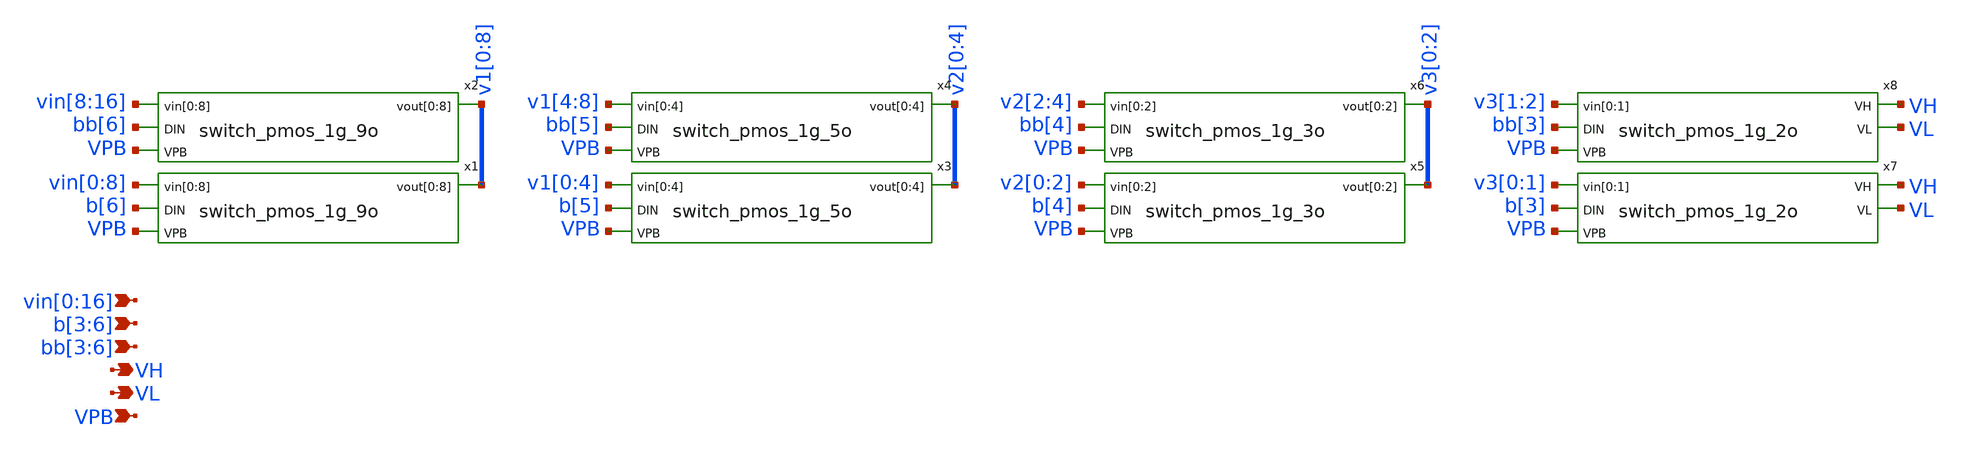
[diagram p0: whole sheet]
** sch_path: xschem/vselector_4b_2v.sch
**.subckt vselector_4b_2v
*+ vin[0],vin[1],vin[2],vin[3],vin[4],vin[5],vin[6],vin[7],vin[8],vin[9],vin[10],vin[11],vin[12],vin[13],vin[14],vin[15],vin[16] VH VPB b[3],b[4],b[5],b[6] VL bb[3],bb[4],bb[5],bb[6]
*.ipin
*+ vin[0],vin[1],vin[2],vin[3],vin[4],vin[5],vin[6],vin[7],vin[8],vin[9],vin[10],vin[11],vin[12],vin[13],vin[14],vin[15],vin[16]
*.opin VH
*.ipin VPB
*.ipin b[3],b[4],b[5],b[6]
*.opin VL
*.ipin bb[3],bb[4],bb[5],bb[6]
x1 vin[0] vin[1] vin[2] vin[3] vin[4] vin[5] vin[6] vin[7] vin[8] b[6] v1[0] v1[1] v1[2] v1[3] v1[4]
+ v1[5] v1[6] v1[7] v1[8] VPB switch_pmos_1g_9o
x2 vin[8] vin[9] vin[10] vin[11] vin[12] vin[13] vin[14] vin[15] vin[16] bb[6] v1[0] v1[1] v1[2]
+ v1[3] v1[4] v1[5] v1[6] v1[7] v1[8] VPB switch_pmos_1g_9o
x3 v1[0] v1[1] v1[2] v1[3] v1[4] b[5] v2[0] v2[1] v2[2] v2[3] v2[4] VPB switch_pmos_1g_5o
x4 v1[4] v1[5] v1[6] v1[7] v1[8] bb[5] v2[0] v2[1] v2[2] v2[3] v2[4] VPB switch_pmos_1g_5o
x5 v2[0] v2[1] v2[2] b[4] v3[0] v3[1] v3[2] VPB switch_pmos_1g_3o
x6 v2[2] v2[3] v2[4] bb[4] v3[0] v3[1] v3[2] VPB switch_pmos_1g_3o
x7 v3[0] v3[1] b[3] VH VL VPB switch_pmos_1g_2o
x8 v3[1] v3[2] bb[3] VH VL VPB switch_pmos_1g_2o
**.ends

* expanding   symbol:  switch_pmos_1g_9o.sym # of pins=4
** sym_path: xschem/switch_pmos_1g_9o.sym
** sch_path: xschem/switch_pmos_1g_9o.sch
.subckt switch_pmos_1g_9o vin[0] vin[1] vin[2] vin[3] vin[4] vin[5] vin[6] vin[7] vin[8] DIN vout[0]
+ vout[1] vout[2] vout[3] vout[4] vout[5] vout[6] vout[7] vout[8] VPB
*.ipin vin[0],vin[1],vin[2],vin[3],vin[4],vin[5],vin[6],vin[7],vin[8]
*.opin vout[0],vout[1],vout[2],vout[3],vout[4],vout[5],vout[6],vout[7],vout[8]
*.ipin VPB
*.ipin DIN
.param wp=0.42 wn=0.42 l=0.5

XM1 vout[0] DIN vin[0] VPB sky130_fd_pr__pfet_g5v0d10v5 L=l W=wp nf=1 ad='int((nf+1)/2) * W/nf * 0.29'
+ as='int((nf+2)/2) * W/nf * 0.29' pd='2*int((nf+1)/2) * (W/nf + 0.29)' ps='2*int((nf+2)/2) * (W/nf + 0.29)'
+ nrd='0.29 / W' nrs='0.29 / W' sa=0 sb=0 sd=0 mult=1 m=1
XM2 vout[1] DIN vin[1] VPB sky130_fd_pr__pfet_g5v0d10v5 L=l W=wp nf=1 ad='int((nf+1)/2) * W/nf * 0.29'
+ as='int((nf+2)/2) * W/nf * 0.29' pd='2*int((nf+1)/2) * (W/nf + 0.29)' ps='2*int((nf+2)/2) * (W/nf + 0.29)'
+ nrd='0.29 / W' nrs='0.29 / W' sa=0 sb=0 sd=0 mult=1 m=1
XM3 vout[2] DIN vin[2] VPB sky130_fd_pr__pfet_g5v0d10v5 L=l W=wp nf=1 ad='int((nf+1)/2) * W/nf * 0.29'
+ as='int((nf+2)/2) * W/nf * 0.29' pd='2*int((nf+1)/2) * (W/nf + 0.29)' ps='2*int((nf+2)/2) * (W/nf + 0.29)'
+ nrd='0.29 / W' nrs='0.29 / W' sa=0 sb=0 sd=0 mult=1 m=1
XM4 vout[3] DIN vin[3] VPB sky130_fd_pr__pfet_g5v0d10v5 L=l W=wp nf=1 ad='int((nf+1)/2) * W/nf * 0.29'
+ as='int((nf+2)/2) * W/nf * 0.29' pd='2*int((nf+1)/2) * (W/nf + 0.29)' ps='2*int((nf+2)/2) * (W/nf + 0.29)'
+ nrd='0.29 / W' nrs='0.29 / W' sa=0 sb=0 sd=0 mult=1 m=1
XM5 vout[4] DIN vin[4] VPB sky130_fd_pr__pfet_g5v0d10v5 L=l W=wp nf=1 ad='int((nf+1)/2) * W/nf * 0.29'
+ as='int((nf+2)/2) * W/nf * 0.29' pd='2*int((nf+1)/2) * (W/nf + 0.29)' ps='2*int((nf+2)/2) * (W/nf + 0.29)'
+ nrd='0.29 / W' nrs='0.29 / W' sa=0 sb=0 sd=0 mult=1 m=1
XM6 vout[5] DIN vin[5] VPB sky130_fd_pr__pfet_g5v0d10v5 L=l W=wp nf=1 ad='int((nf+1)/2) * W/nf * 0.29'
+ as='int((nf+2)/2) * W/nf * 0.29' pd='2*int((nf+1)/2) * (W/nf + 0.29)' ps='2*int((nf+2)/2) * (W/nf + 0.29)'
+ nrd='0.29 / W' nrs='0.29 / W' sa=0 sb=0 sd=0 mult=1 m=1
XM7 vout[6] DIN vin[6] VPB sky130_fd_pr__pfet_g5v0d10v5 L=l W=wp nf=1 ad='int((nf+1)/2) * W/nf * 0.29'
+ as='int((nf+2)/2) * W/nf * 0.29' pd='2*int((nf+1)/2) * (W/nf + 0.29)' ps='2*int((nf+2)/2) * (W/nf + 0.29)'
+ nrd='0.29 / W' nrs='0.29 / W' sa=0 sb=0 sd=0 mult=1 m=1
XM8 vout[7] DIN vin[7] VPB sky130_fd_pr__pfet_g5v0d10v5 L=l W=wp nf=1 ad='int((nf+1)/2) * W/nf * 0.29'
+ as='int((nf+2)/2) * W/nf * 0.29' pd='2*int((nf+1)/2) * (W/nf + 0.29)' ps='2*int((nf+2)/2) * (W/nf + 0.29)'
+ nrd='0.29 / W' nrs='0.29 / W' sa=0 sb=0 sd=0 mult=1 m=1
XM9 vout[8] DIN vin[8] VPB sky130_fd_pr__pfet_g5v0d10v5 L=l W=wp nf=1 ad='int((nf+1)/2) * W/nf * 0.29'
+ as='int((nf+2)/2) * W/nf * 0.29' pd='2*int((nf+1)/2) * (W/nf + 0.29)' ps='2*int((nf+2)/2) * (W/nf + 0.29)'
+ nrd='0.29 / W' nrs='0.29 / W' sa=0 sb=0 sd=0 mult=1 m=1
.ends


* expanding   symbol:  switch_pmos_1g_5o.sym # of pins=4
** sym_path: xschem/switch_pmos_1g_5o.sym
** sch_path: xschem/switch_pmos_1g_5o.sch
.subckt switch_pmos_1g_5o vin[0] vin[1] vin[2] vin[3] vin[4] DIN vout[0] vout[1] vout[2] vout[3]
+ vout[4] VPB
*.ipin vin[0],vin[1],vin[2],vin[3],vin[4]
*.opin vout[0],vout[1],vout[2],vout[3],vout[4]
*.ipin VPB
*.ipin DIN
.param wp=0.42 wn=0.42 l=0.5

XM1 vout[0] DIN vin[0] VPB sky130_fd_pr__pfet_g5v0d10v5 L=l W=wp nf=1 ad='int((nf+1)/2) * W/nf * 0.29'
+ as='int((nf+2)/2) * W/nf * 0.29' pd='2*int((nf+1)/2) * (W/nf + 0.29)' ps='2*int((nf+2)/2) * (W/nf + 0.29)'
+ nrd='0.29 / W' nrs='0.29 / W' sa=0 sb=0 sd=0 mult=1 m=1
XM2 vout[1] DIN vin[1] VPB sky130_fd_pr__pfet_g5v0d10v5 L=l W=wp nf=1 ad='int((nf+1)/2) * W/nf * 0.29'
+ as='int((nf+2)/2) * W/nf * 0.29' pd='2*int((nf+1)/2) * (W/nf + 0.29)' ps='2*int((nf+2)/2) * (W/nf + 0.29)'
+ nrd='0.29 / W' nrs='0.29 / W' sa=0 sb=0 sd=0 mult=1 m=1
XM3 vout[2] DIN vin[2] VPB sky130_fd_pr__pfet_g5v0d10v5 L=l W=wp nf=1 ad='int((nf+1)/2) * W/nf * 0.29'
+ as='int((nf+2)/2) * W/nf * 0.29' pd='2*int((nf+1)/2) * (W/nf + 0.29)' ps='2*int((nf+2)/2) * (W/nf + 0.29)'
+ nrd='0.29 / W' nrs='0.29 / W' sa=0 sb=0 sd=0 mult=1 m=1
XM4 vout[3] DIN vin[3] VPB sky130_fd_pr__pfet_g5v0d10v5 L=l W=wp nf=1 ad='int((nf+1)/2) * W/nf * 0.29'
+ as='int((nf+2)/2) * W/nf * 0.29' pd='2*int((nf+1)/2) * (W/nf + 0.29)' ps='2*int((nf+2)/2) * (W/nf + 0.29)'
+ nrd='0.29 / W' nrs='0.29 / W' sa=0 sb=0 sd=0 mult=1 m=1
XM5 vout[4] DIN vin[4] VPB sky130_fd_pr__pfet_g5v0d10v5 L=l W=wp nf=1 ad='int((nf+1)/2) * W/nf * 0.29'
+ as='int((nf+2)/2) * W/nf * 0.29' pd='2*int((nf+1)/2) * (W/nf + 0.29)' ps='2*int((nf+2)/2) * (W/nf + 0.29)'
+ nrd='0.29 / W' nrs='0.29 / W' sa=0 sb=0 sd=0 mult=1 m=1
.ends


* expanding   symbol:  switch_pmos_1g_3o.sym # of pins=4
** sym_path: xschem/switch_pmos_1g_3o.sym
** sch_path: xschem/switch_pmos_1g_3o.sch
.subckt switch_pmos_1g_3o vin[0] vin[1] vin[2] DIN vout[0] vout[1] vout[2] VPB
*.ipin vin[0],vin[1],vin[2]
*.opin vout[0],vout[1],vout[2]
*.ipin VPB
*.ipin DIN
.param wp=0.42 wn=0.42 l=0.5

XM1 vout[0] DIN vin[0] VPB sky130_fd_pr__pfet_g5v0d10v5 L=l W=wp nf=1 ad='int((nf+1)/2) * W/nf * 0.29'
+ as='int((nf+2)/2) * W/nf * 0.29' pd='2*int((nf+1)/2) * (W/nf + 0.29)' ps='2*int((nf+2)/2) * (W/nf + 0.29)'
+ nrd='0.29 / W' nrs='0.29 / W' sa=0 sb=0 sd=0 mult=1 m=1
XM2 vout[1] DIN vin[1] VPB sky130_fd_pr__pfet_g5v0d10v5 L=l W=wp nf=1 ad='int((nf+1)/2) * W/nf * 0.29'
+ as='int((nf+2)/2) * W/nf * 0.29' pd='2*int((nf+1)/2) * (W/nf + 0.29)' ps='2*int((nf+2)/2) * (W/nf + 0.29)'
+ nrd='0.29 / W' nrs='0.29 / W' sa=0 sb=0 sd=0 mult=1 m=1
XM3 vout[2] DIN vin[2] VPB sky130_fd_pr__pfet_g5v0d10v5 L=l W=wp nf=1 ad='int((nf+1)/2) * W/nf * 0.29'
+ as='int((nf+2)/2) * W/nf * 0.29' pd='2*int((nf+1)/2) * (W/nf + 0.29)' ps='2*int((nf+2)/2) * (W/nf + 0.29)'
+ nrd='0.29 / W' nrs='0.29 / W' sa=0 sb=0 sd=0 mult=1 m=1
.ends


* expanding   symbol:  switch_pmos_1g_2o.sym # of pins=5
** sym_path: xschem/switch_pmos_1g_2o.sym
** sch_path: xschem/switch_pmos_1g_2o.sch
.subckt switch_pmos_1g_2o vin[0] vin[1] DIN VH VL VPB
*.ipin vin[0],vin[1]
*.opin VH
*.ipin VPB
*.ipin DIN
*.opin VL
.param wp=0.42 wn=0.42 l=0.5

XM1 VL DIN vin[0] VPB sky130_fd_pr__pfet_g5v0d10v5 L=l W=wp nf=1 ad='int((nf+1)/2) * W/nf * 0.29' as='int((nf+2)/2) * W/nf * 0.29'
+ pd='2*int((nf+1)/2) * (W/nf + 0.29)' ps='2*int((nf+2)/2) * (W/nf + 0.29)' nrd='0.29 / W' nrs='0.29 / W'
+ sa=0 sb=0 sd=0 mult=1 m=1
XM2 VH DIN vin[1] VPB sky130_fd_pr__pfet_g5v0d10v5 L=l W=wp nf=1 ad='int((nf+1)/2) * W/nf * 0.29' as='int((nf+2)/2) * W/nf * 0.29'
+ pd='2*int((nf+1)/2) * (W/nf + 0.29)' ps='2*int((nf+2)/2) * (W/nf + 0.29)' nrd='0.29 / W' nrs='0.29 / W'
+ sa=0 sb=0 sd=0 mult=1 m=1
.ends

.end
